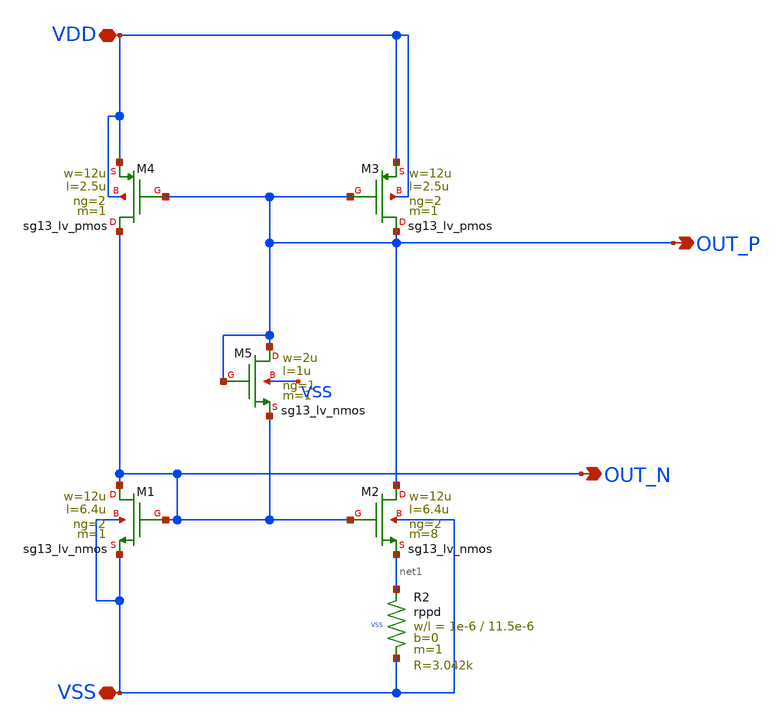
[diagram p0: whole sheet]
** sch_path: OTA_Telescopic_v1/OTA_Telescopic_currentRef.sch
**.subckt OTA_Telescopic_currentRef VDD VSS OUT_P OUT_N
*.iopin VDD
*.iopin VSS
*.opin OUT_P
*.opin OUT_N
XM3 OUT_P OUT_P VDD VDD sg13_lv_pmos w=12u l=2.5u ng=2 m=1 mm_ok=1
XM2 OUT_P OUT_N net1 VSS sg13_lv_nmos w=12u l=6.4u ng=2 m=8 mm_ok=1
XM4 OUT_N OUT_P VDD VDD sg13_lv_pmos w=12u l=2.5u ng=2 m=1 mm_ok=1
XM1 OUT_N OUT_N VSS VSS sg13_lv_nmos w=12u l=6.4u ng=2 m=1 mm_ok=1
XM5 OUT_P OUT_P OUT_N VSS sg13_lv_nmos w=2u l=1u ng=1 m=1 mm_ok=1
XR2 net1 VSS VSS rppd w=1e-6 l=11.5e-6 m=1 b=0 mm_ok=1
**.ends
.end
